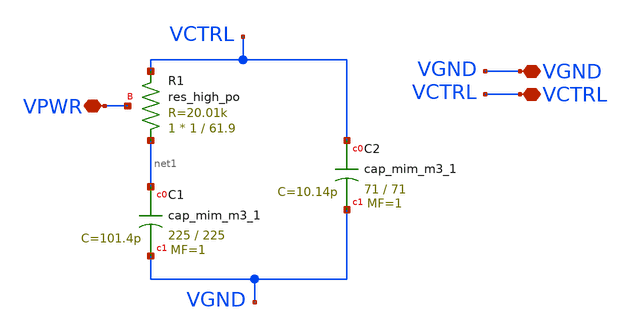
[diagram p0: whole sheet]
** sch_path: lf.sch
**.subckt lf VGND VCTRL VPWR
*.iopin VGND
*.iopin VCTRL
*.iopin VPWR
XC1 net1 VGND sky130_fd_pr__cap_mim_m3_1 W=225 L=225 MF=1 m=1
XC2 VCTRL VGND sky130_fd_pr__cap_mim_m3_1 W=71 L=71 MF=1 m=1
XR1 net1 VCTRL VPWR sky130_fd_pr__res_high_po W=1 L=61.9 mult=1 m=1
**.ends
.end
